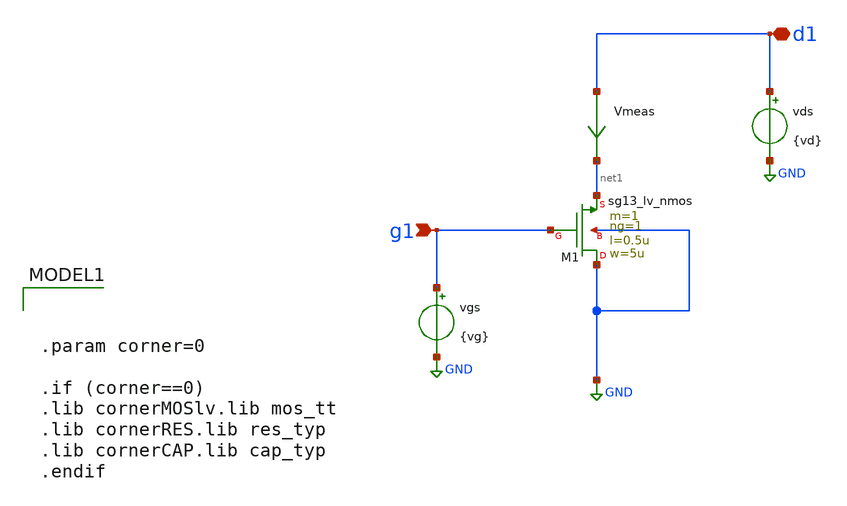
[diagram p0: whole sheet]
** sch_path: Tarea_1/xschem/lv_mos_characterization.sch
**.subckt lv_mos_characterization g1 d1
*.ipin g1
*.iopin d1
XM1 GND g1 net1 GND sg13_lv_nmos w=5u l=0.5u ng=1 m=1 mm_ok=1
Vmeas d1 net1 0
.save i(vmeas)
vgs g1 GND {vg}
vds d1 GND {vd}
**** begin user architecture code


.param corner=0

.if (corner==0)
.lib cornerMOSlv.lib mos_tt
.lib cornerRES.lib res_typ
.lib cornerCAP.lib cap_typ
.endif



.param vd = 0.75
.param vg = 0.75
.control
save all
save @n.xm1.nsg13_lv_nmos[ids]
save @n.xm1.nsg13_lv_nmos[gm]
save @n.xm1.nsg13_lv_nmos[vth]
save @n.xm1.nsg13_lv_nmos[cgg]
save @n.xm1.nsg13_lv_nmos[cgsol]
save @n.xm1.nsg13_lv_nmos[cgdol]
save @n.xm1.nsg13_lv_nmos[vgs]
save @n.xm1.nsg13_lv_nmos[vdss]

dc vgs 0.01 1.8 0.01 vds 0.4 1.35 0.05

let idn = @n.xm1.nsg13_lv_nmos[ids]
let gmn = @n.xm1.nsg13_lv_nmos[gm]
let vthn = @n.xm1.nsg13_lv_nmos[vth]
let vgsn = @n.xm1.nsg13_lv_nmos[vgs]
let vdsatn = @n.xm1.nsg13_lv_nmos[vdss]

let cgg = @n.xm1.nsg13_lv_nmos[cgg]
let cgsol = @n.xm1.nsg13_lv_nmos[cgsol]
let cgdol = @n.xm1.nsg13_lv_nmos[cgdol]
let c_tot = cgg + cgsol + cgdol
let ft = gmn/(2*pi*c_tot)

let vov = 2*idn/gmn
let vov2 = vgsn - vthn
*Vov teorico difiere demasiado con vov real
*Vov=2.38 cuando vgs=1.8, siendo que Vthn = .27 (Vov irrealista, no aplicable)
*print vov2
let gmoverId = gmn/idn

*plot idn title A_lineal
*plot ylog idn title A_log
*plot gmn
*plot xlog gmoverId

wrdata nmos_char_idn.raw idn

wrdata nmos_char_gmid-vov.raw gmoverID vov2

wrdata nmos_char_gmid-ft.raw gmoverId ft
*print vthn

dc vds 0.0 1.35 0.01 vgs 0.4 1.5 0.1
let idn = @n.xm1.nsg13_lv_nmos[ids]
wrdata nmos_char_vds.raw idn
.endc


**** end user architecture code
**.ends
.GLOBAL GND
.end
